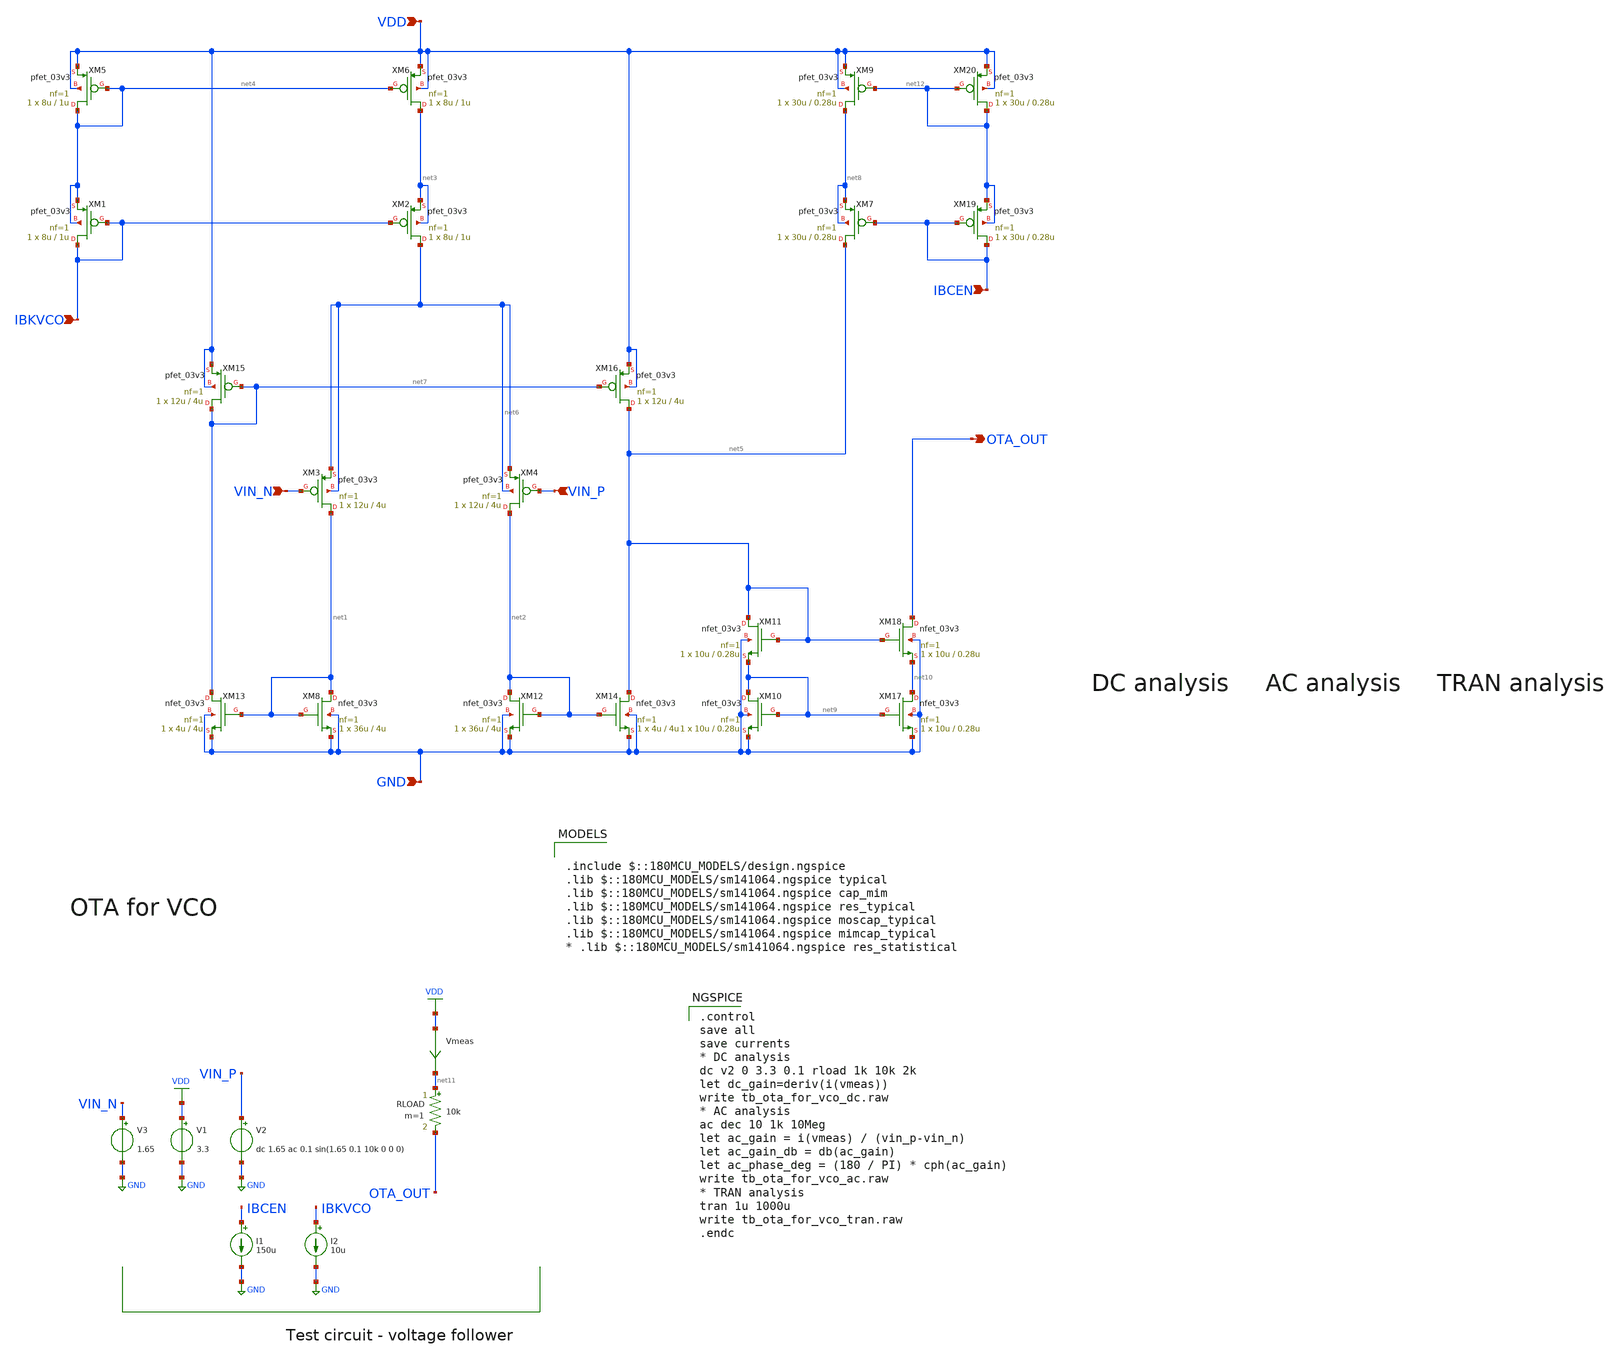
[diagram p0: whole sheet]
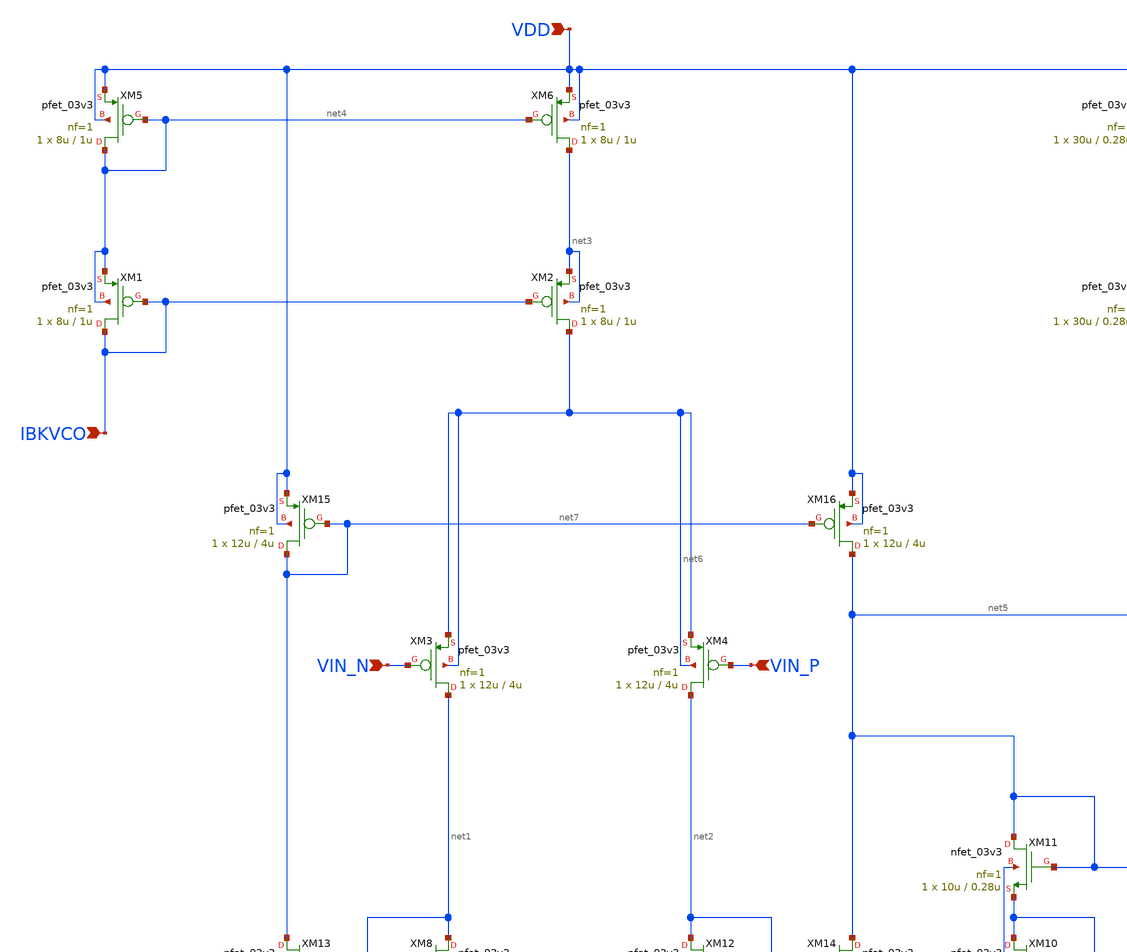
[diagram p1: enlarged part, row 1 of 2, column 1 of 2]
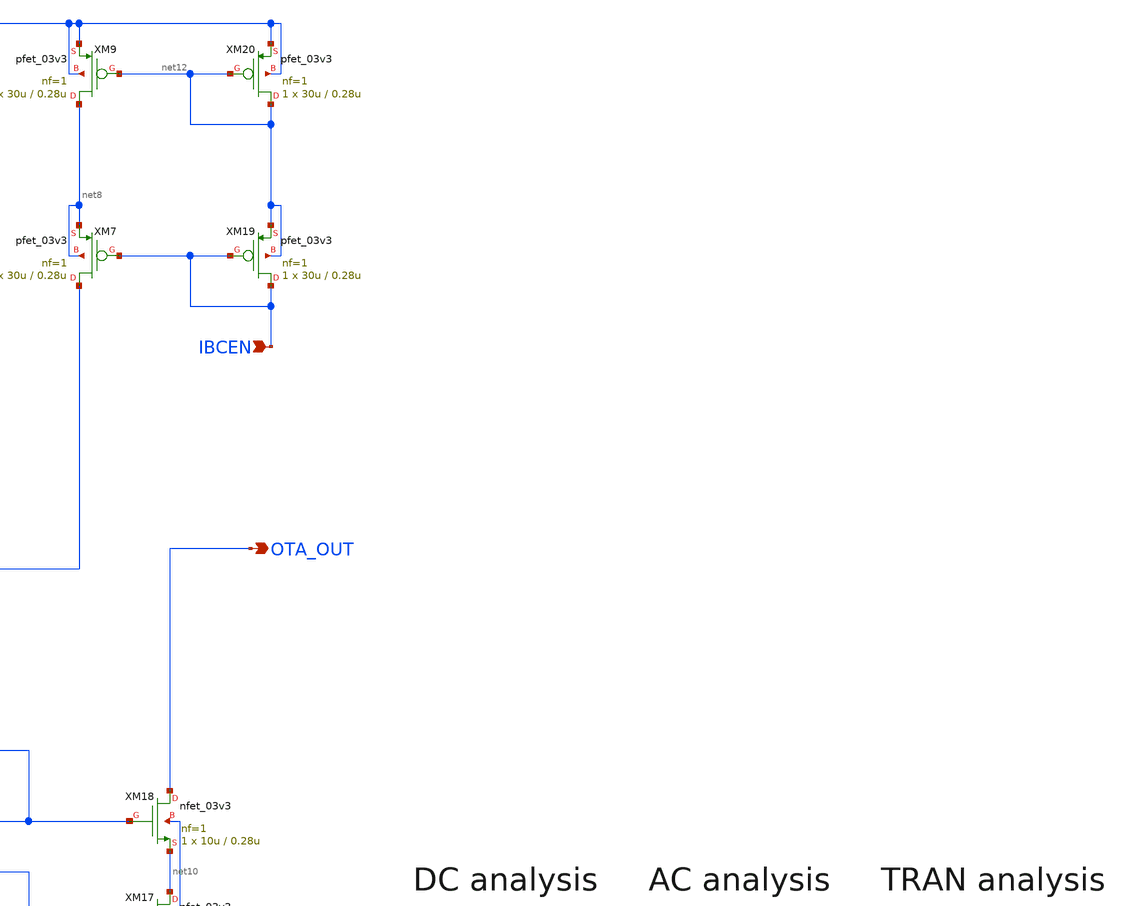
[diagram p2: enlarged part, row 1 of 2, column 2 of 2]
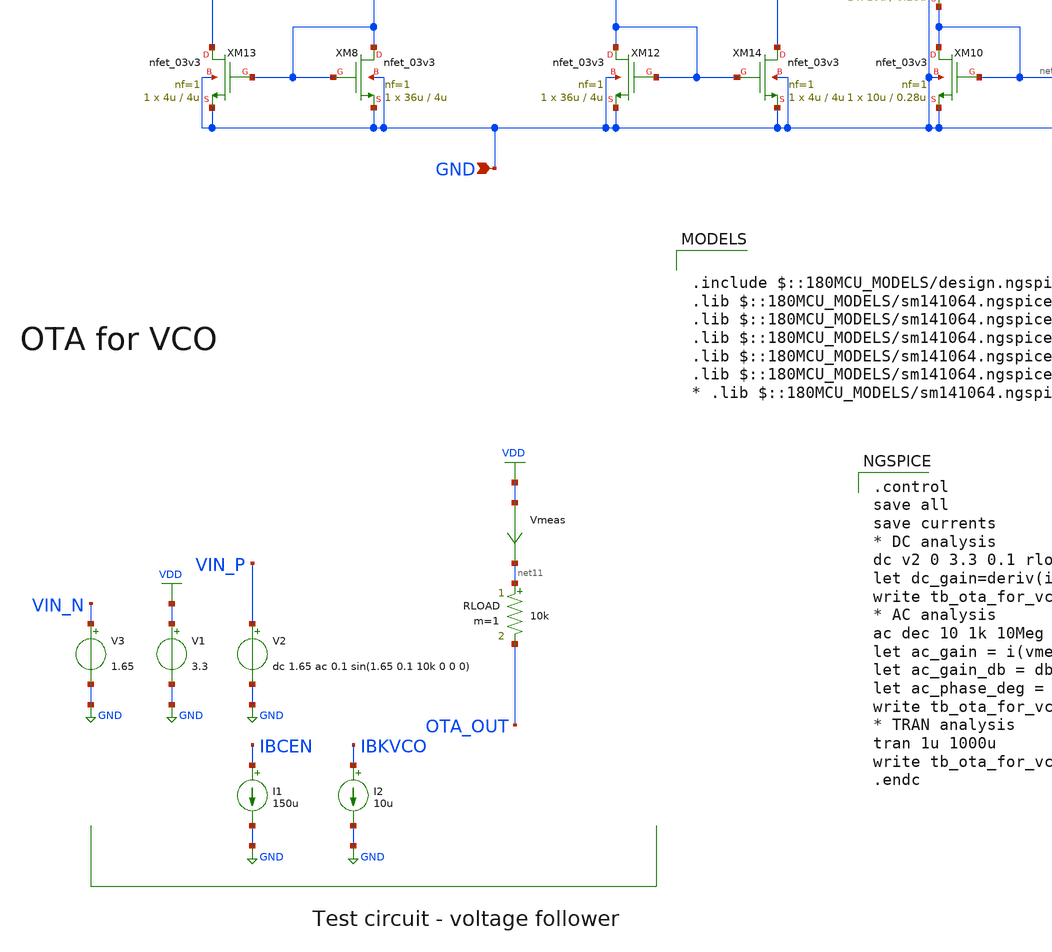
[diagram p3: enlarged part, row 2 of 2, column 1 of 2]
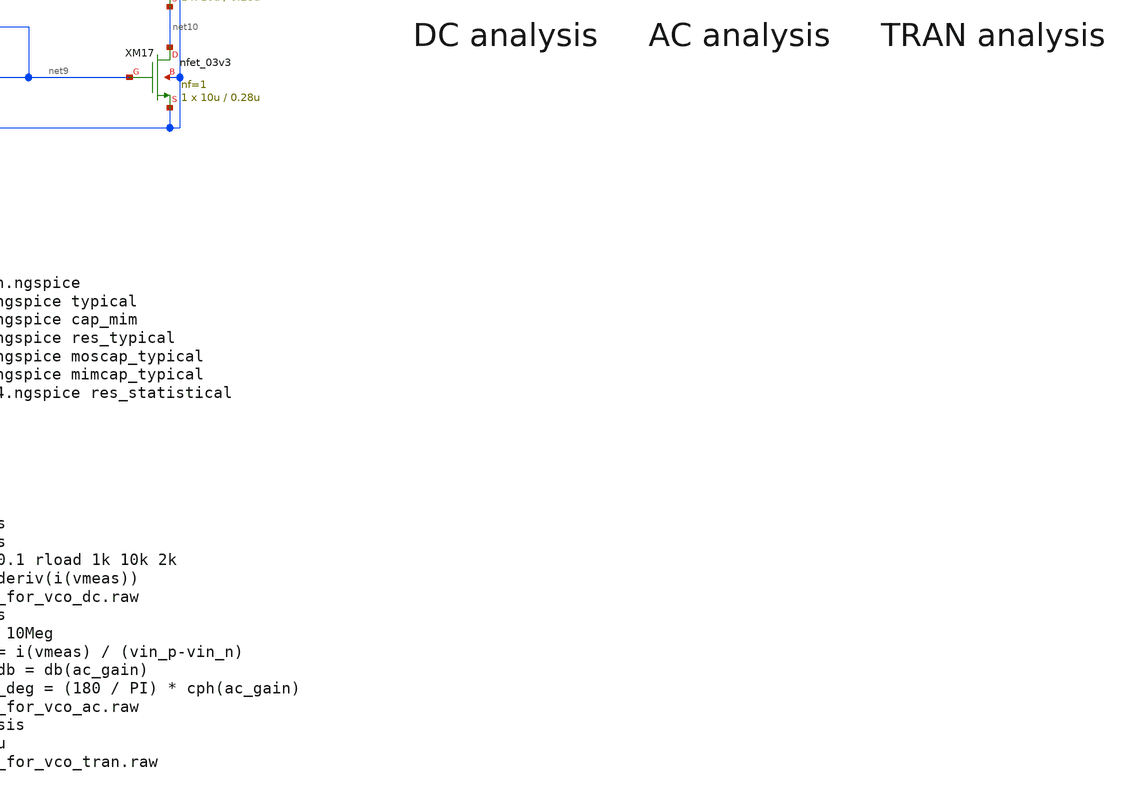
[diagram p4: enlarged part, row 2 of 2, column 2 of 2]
** sch_path: designs/libs/tb_analog/tb_ota_for_vco/tb_ota_for_vco.sch
* Copyright 2022 GlobalFoundries PDK Authors
* Licensed under the Apache License, Version 2.0 (the "License");
* you may not use this file except in compliance with the License.
* You may obtain a copy of the License at
* https://www.apache.org/licenses/LICENSE-2.0
* Unless required by applicable law or agreed to in writing, software
* distributed under the License is distributed on an "AS IS" BASIS,
* WITHOUT WARRANTIES OR CONDITIONS OF ANY KIND, either express or implied.
* See the License for the specific language governing permissions and
* limitations under the License.
**.subckt tb_ota_for_vco IBKVCO VIN_N VIN_P OTA_OUT GND VDD IBCEN
*.ipin IBKVCO
*.ipin VIN_N
*.ipin VIN_P
*.opin OTA_OUT
*.ipin GND
*.ipin VDD
*.ipin IBCEN
V1 VDD GND 3.3
I1 IBCEN GND 150u
V2 VIN_P GND dc 1.65 ac 0.1 sin(1.65 0.1 10k 0 0 0)
V3 VIN_N GND 1.65
RLOAD net11 OTA_OUT 10k m=1
Vmeas VDD net11 0
.save i(vmeas)
XM1 IBKVCO IBKVCO net4 net4 pfet_03v3 L=1u W=8u nf=1 ad='int((nf+1)/2) * W/nf * 0.18u' as='int((nf+2)/2) * W/nf * 0.18u'
+ pd='2*int((nf+1)/2) * (W/nf + 0.18u)' ps='2*int((nf+2)/2) * (W/nf + 0.18u)' nrd='0.18u / W' nrs='0.18u / W'
+ sa=0 sb=0 sd=0 m=1
XM2 net6 IBKVCO net3 net3 pfet_03v3 L=1u W=8u nf=1 ad='int((nf+1)/2) * W/nf * 0.18u' as='int((nf+2)/2) * W/nf * 0.18u'
+ pd='2*int((nf+1)/2) * (W/nf + 0.18u)' ps='2*int((nf+2)/2) * (W/nf + 0.18u)' nrd='0.18u / W' nrs='0.18u / W'
+ sa=0 sb=0 sd=0 m=1
XM3 net1 VIN_N net6 net6 pfet_03v3 L=4u W=12u nf=1 ad='int((nf+1)/2) * W/nf * 0.18u' as='int((nf+2)/2) * W/nf * 0.18u'
+ pd='2*int((nf+1)/2) * (W/nf + 0.18u)' ps='2*int((nf+2)/2) * (W/nf + 0.18u)' nrd='0.18u / W' nrs='0.18u / W'
+ sa=0 sb=0 sd=0 m=1
XM4 net2 VIN_P net6 net6 pfet_03v3 L=4u W=12u nf=1 ad='int((nf+1)/2) * W/nf * 0.18u' as='int((nf+2)/2) * W/nf * 0.18u'
+ pd='2*int((nf+1)/2) * (W/nf + 0.18u)' ps='2*int((nf+2)/2) * (W/nf + 0.18u)' nrd='0.18u / W' nrs='0.18u / W'
+ sa=0 sb=0 sd=0 m=1
XM8 net1 net1 GND GND nfet_03v3 L=4u W=36u nf=1 ad='int((nf+1)/2) * W/nf * 0.18u' as='int((nf+2)/2) * W/nf * 0.18u'
+ pd='2*int((nf+1)/2) * (W/nf + 0.18u)' ps='2*int((nf+2)/2) * (W/nf + 0.18u)' nrd='0.18u / W' nrs='0.18u / W'
+ sa=0 sb=0 sd=0 m=1
XM12 net2 net2 GND GND nfet_03v3 L=4u W=36u nf=1 ad='int((nf+1)/2) * W/nf * 0.18u' as='int((nf+2)/2) * W/nf * 0.18u'
+ pd='2*int((nf+1)/2) * (W/nf + 0.18u)' ps='2*int((nf+2)/2) * (W/nf + 0.18u)' nrd='0.18u / W' nrs='0.18u / W'
+ sa=0 sb=0 sd=0 m=1
XM13 net7 net1 GND GND nfet_03v3 L=4u W=4u nf=1 ad='int((nf+1)/2) * W/nf * 0.18u' as='int((nf+2)/2) * W/nf * 0.18u'
+ pd='2*int((nf+1)/2) * (W/nf + 0.18u)' ps='2*int((nf+2)/2) * (W/nf + 0.18u)' nrd='0.18u / W' nrs='0.18u / W'
+ sa=0 sb=0 sd=0 m=1
XM14 net5 net2 GND GND nfet_03v3 L=4u W=4u nf=1 ad='int((nf+1)/2) * W/nf * 0.18u' as='int((nf+2)/2) * W/nf * 0.18u'
+ pd='2*int((nf+1)/2) * (W/nf + 0.18u)' ps='2*int((nf+2)/2) * (W/nf + 0.18u)' nrd='0.18u / W' nrs='0.18u / W'
+ sa=0 sb=0 sd=0 m=1
XM15 net7 net7 VDD VDD pfet_03v3 L=4u W=12u nf=1 ad='int((nf+1)/2) * W/nf * 0.18u' as='int((nf+2)/2) * W/nf * 0.18u'
+ pd='2*int((nf+1)/2) * (W/nf + 0.18u)' ps='2*int((nf+2)/2) * (W/nf + 0.18u)' nrd='0.18u / W' nrs='0.18u / W'
+ sa=0 sb=0 sd=0 m=1
XM16 net5 net7 VDD VDD pfet_03v3 L=4u W=12u nf=1 ad='int((nf+1)/2) * W/nf * 0.18u' as='int((nf+2)/2) * W/nf * 0.18u'
+ pd='2*int((nf+1)/2) * (W/nf + 0.18u)' ps='2*int((nf+2)/2) * (W/nf + 0.18u)' nrd='0.18u / W' nrs='0.18u / W'
+ sa=0 sb=0 sd=0 m=1
XM5 net4 net4 VDD VDD pfet_03v3 L=1u W=8u nf=1 ad='int((nf+1)/2) * W/nf * 0.18u' as='int((nf+2)/2) * W/nf * 0.18u'
+ pd='2*int((nf+1)/2) * (W/nf + 0.18u)' ps='2*int((nf+2)/2) * (W/nf + 0.18u)' nrd='0.18u / W' nrs='0.18u / W'
+ sa=0 sb=0 sd=0 m=1
XM6 net3 net4 VDD VDD pfet_03v3 L=1u W=8u nf=1 ad='int((nf+1)/2) * W/nf * 0.18u' as='int((nf+2)/2) * W/nf * 0.18u'
+ pd='2*int((nf+1)/2) * (W/nf + 0.18u)' ps='2*int((nf+2)/2) * (W/nf + 0.18u)' nrd='0.18u / W' nrs='0.18u / W'
+ sa=0 sb=0 sd=0 m=1
XM7 net5 IBCEN net8 net8 pfet_03v3 L=0.28u W=30u nf=1 ad='int((nf+1)/2) * W/nf * 0.18u' as='int((nf+2)/2) * W/nf * 0.18u'
+ pd='2*int((nf+1)/2) * (W/nf + 0.18u)' ps='2*int((nf+2)/2) * (W/nf + 0.18u)' nrd='0.18u / W' nrs='0.18u / W'
+ sa=0 sb=0 sd=0 m=1
XM9 net8 net12 VDD VDD pfet_03v3 L=0.28u W=30u nf=1 ad='int((nf+1)/2) * W/nf * 0.18u' as='int((nf+2)/2) * W/nf * 0.18u'
+ pd='2*int((nf+1)/2) * (W/nf + 0.18u)' ps='2*int((nf+2)/2) * (W/nf + 0.18u)' nrd='0.18u / W' nrs='0.18u / W'
+ sa=0 sb=0 sd=0 m=1
XM10 net9 net9 GND GND nfet_03v3 L=0.28u W=10u nf=1 ad='int((nf+1)/2) * W/nf * 0.18u' as='int((nf+2)/2) * W/nf * 0.18u'
+ pd='2*int((nf+1)/2) * (W/nf + 0.18u)' ps='2*int((nf+2)/2) * (W/nf + 0.18u)' nrd='0.18u / W' nrs='0.18u / W'
+ sa=0 sb=0 sd=0 m=1
XM11 net5 net5 net9 GND nfet_03v3 L=0.28u W=10u nf=1 ad='int((nf+1)/2) * W/nf * 0.18u' as='int((nf+2)/2) * W/nf * 0.18u'
+ pd='2*int((nf+1)/2) * (W/nf + 0.18u)' ps='2*int((nf+2)/2) * (W/nf + 0.18u)' nrd='0.18u / W' nrs='0.18u / W'
+ sa=0 sb=0 sd=0 m=1
XM17 net10 net9 GND GND nfet_03v3 L=0.28u W=10u nf=1 ad='int((nf+1)/2) * W/nf * 0.18u' as='int((nf+2)/2) * W/nf * 0.18u'
+ pd='2*int((nf+1)/2) * (W/nf + 0.18u)' ps='2*int((nf+2)/2) * (W/nf + 0.18u)' nrd='0.18u / W' nrs='0.18u / W'
+ sa=0 sb=0 sd=0 m=1
XM18 OTA_OUT net5 net10 GND nfet_03v3 L=0.28u W=10u nf=1 ad='int((nf+1)/2) * W/nf * 0.18u' as='int((nf+2)/2) * W/nf * 0.18u'
+ pd='2*int((nf+1)/2) * (W/nf + 0.18u)' ps='2*int((nf+2)/2) * (W/nf + 0.18u)' nrd='0.18u / W' nrs='0.18u / W'
+ sa=0 sb=0 sd=0 m=1
XM19 IBCEN IBCEN net12 net12 pfet_03v3 L=0.28u W=30u nf=1 ad='int((nf+1)/2) * W/nf * 0.18u' as='int((nf+2)/2) * W/nf * 0.18u'
+ pd='2*int((nf+1)/2) * (W/nf + 0.18u)' ps='2*int((nf+2)/2) * (W/nf + 0.18u)' nrd='0.18u / W' nrs='0.18u / W'
+ sa=0 sb=0 sd=0 m=1
XM20 net12 net12 VDD VDD pfet_03v3 L=0.28u W=30u nf=1 ad='int((nf+1)/2) * W/nf * 0.18u' as='int((nf+2)/2) * W/nf * 0.18u'
+ pd='2*int((nf+1)/2) * (W/nf + 0.18u)' ps='2*int((nf+2)/2) * (W/nf + 0.18u)' nrd='0.18u / W' nrs='0.18u / W'
+ sa=0 sb=0 sd=0 m=1
I2 IBKVCO GND 10u
**** begin user architecture code

.control
save all
save currents
* DC analysis
dc v2 0 3.3 0.1 rload 1k 10k 2k
let dc_gain=deriv(i(vmeas))
write tb_ota_for_vco_dc.raw
* AC analysis
ac dec 10 1k 10Meg
let ac_gain = i(vmeas) / (vin_p-vin_n)
let ac_gain_db = db(ac_gain)
let ac_phase_deg = (180 / PI) * cph(ac_gain)
write tb_ota_for_vco_ac.raw
* TRAN analysis
tran 1u 1000u
write tb_ota_for_vco_tran.raw
.endc



.include $::180MCU_MODELS/design.ngspice
.lib $::180MCU_MODELS/sm141064.ngspice typical
.lib $::180MCU_MODELS/sm141064.ngspice cap_mim
.lib $::180MCU_MODELS/sm141064.ngspice res_typical
.lib $::180MCU_MODELS/sm141064.ngspice moscap_typical
.lib $::180MCU_MODELS/sm141064.ngspice mimcap_typical
* .lib $::180MCU_MODELS/sm141064.ngspice res_statistical

**** end user architecture code
**.ends
.GLOBAL VDD
.GLOBAL GND
.end
